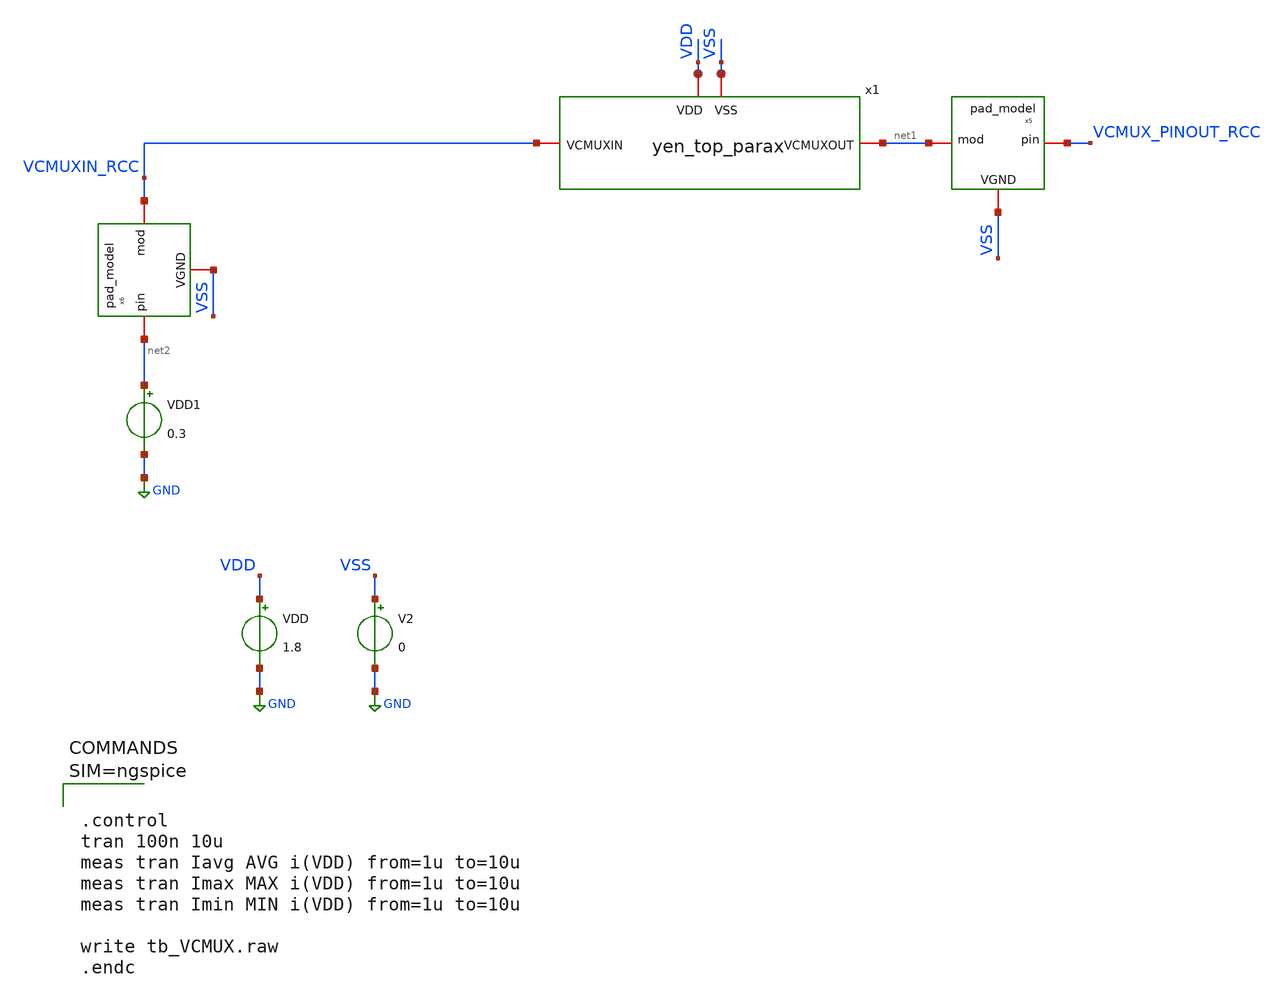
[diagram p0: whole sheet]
** sch_path: xschem/untitled.sch
**.subckt untitled
V2 VSS GND 0
VDD VDD GND 1.8
x1 VDD VSS VCMUXIN_RCC net1 yen_top_parax
x5 VSS VCMUX_PINOUT_RCC net1 pad_model
x6 VSS net2 VCMUXIN_RCC pad_model
VDD1 net2 GND 0.3
**** begin user architecture code

** opencircuitdesign pdks install
.lib $::SKYWATER_MODELS/sky130.lib.spice ff





.control
tran 100n 10u
meas tran Iavg AVG i(VDD) from=1u to=10u
meas tran Imax MAX i(VDD) from=1u to=10u
meas tran Imin MIN i(VDD) from=1u to=10u

write tb_VCMUX.raw
.endc



**** end user architecture code
**.ends
.GLOBAL GND
.end
